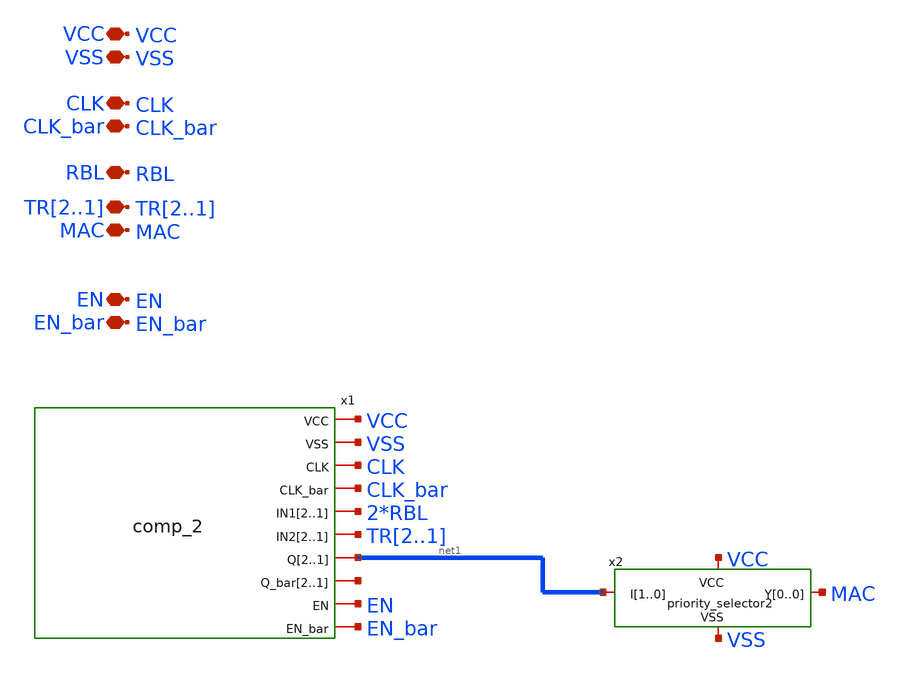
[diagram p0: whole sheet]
** sch_path: voltage_comp/MAC_decoder_7.sch
**.subckt MAC_decoder_7 VSS VCC CLK CLK_bar EN EN_bar MAC TR2,TR1 RBL
*.iopin VSS
*.iopin VCC
*.iopin CLK
*.iopin CLK_bar
*.iopin EN
*.iopin EN_bar
*.iopin MAC
*.iopin TR2,TR1
*.iopin RBL
x1 VCC VSS CLK CLK_bar RBL RBL TR2 TR1 net1[1] net1[0] net2[1] net2[0] EN EN_bar comp_2
x2 VCC VSS net1[1] net1[0] MAC priority_selector2
**.ends
.end
